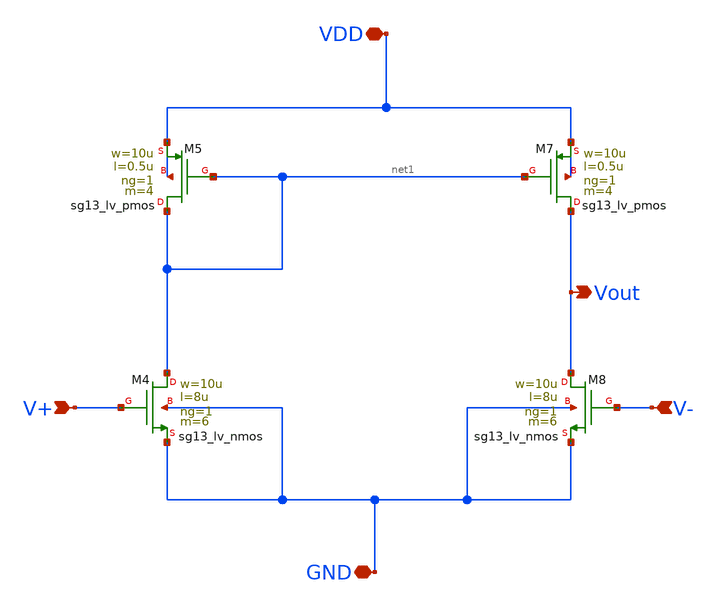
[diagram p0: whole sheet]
** sch_path: SSDOR_1.2V_v4/components/Ibias_uA/ibias_opamp/Ib_opamp.sch
**.subckt Ib_opamp VDD V+ V- GND Vout
*.iopin VDD
*.ipin V+
*.ipin V-
*.iopin GND
*.opin Vout
XM4 net1 V+ GND GND sg13_lv_nmos w=10u l=8u ng=1 m=6 mm_ok=1
XM5 net1 net1 VDD VDD sg13_lv_pmos w=10u l=0.5u ng=1 m=4 mm_ok=1
XM7 Vout net1 VDD VDD sg13_lv_pmos w=10u l=0.5u ng=1 m=4 mm_ok=1
XM8 Vout V- GND GND sg13_lv_nmos w=10u l=8u ng=1 m=6 mm_ok=1
**.ends
.end
